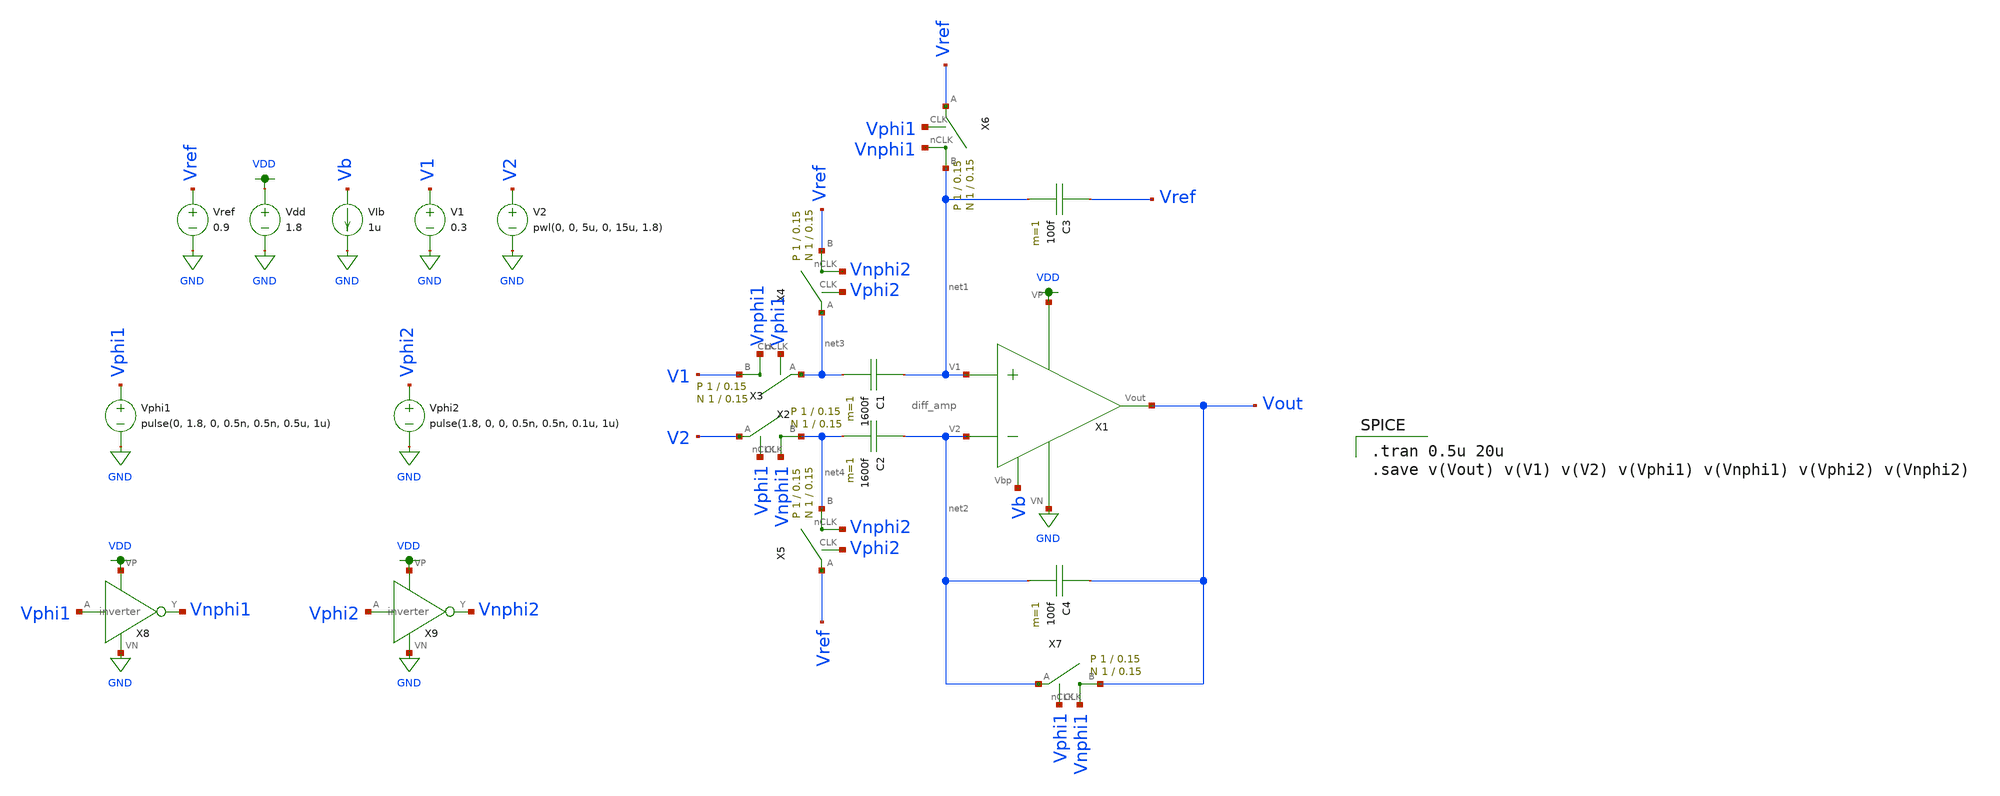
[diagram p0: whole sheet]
** sch_path: schematic/archive/alpha_amp_new.sch
**.subckt alpha_amp_new
X1 VDD Vb Vout net1 net2 GND diff_amp
C1 net1 net3 1600f m=1
C2 net2 net4 1600f m=1
C3 Vref net1 100f m=1
C4 Vout net2 100f m=1
X2 V1 net3 Vphi1 Vnphi1 switch Wp=1 Lp=0.15 WW=1 LL=0.15
X3 net4 V2 Vphi1 Vnphi1 switch Wp=1 Lp=0.15 WW=1 LL=0.15
X4 Vref net3 Vphi2 Vnphi2 switch Wp=1 Lp=0.15 WW=1 LL=0.15
X5 net4 Vref Vphi2 Vnphi2 switch Wp=1 Lp=0.15 WW=1 LL=0.15
X6 net1 Vref Vphi1 Vnphi1 switch Wp=1 Lp=0.15 WW=1 LL=0.15
X7 Vout net2 Vphi1 Vnphi1 switch Wp=1 Lp=0.15 WW=1 LL=0.15
Vdd VDD GND 1.8
V1 V1 GND 0.3
V2 V2 GND pwl(0, 0, 5u, 0, 15u, 1.8)
Vphi1 Vphi1 GND pulse(0, 1.8, 0, 0.5n, 0.5n, 0.5u, 1u)
VIb Vb GND 1u
X8 Vphi1 Vnphi1 VDD GND inverter
Vphi2 Vphi2 GND pulse(1.8, 0, 0, 0.5n, 0.5n, 0.1u, 1u)
X9 Vphi2 Vnphi2 VDD GND inverter
Vref Vref GND 0.9
**** begin user architecture code

.option wnflag=1
.param MC_SWITCH=0.0
.lib ~/skywater/skywater-pdk/libraries/sky130_fd_pr_ngspice/latest/models/sky130.lib.spice tt


.tran 0.5u 20u
.save v(Vout) v(V1) v(V2) v(Vphi1) v(Vnphi1) v(Vphi2) v(Vnphi2)

**** end user architecture code
**.ends
.GLOBAL GND
.GLOBAL VDD
.end
